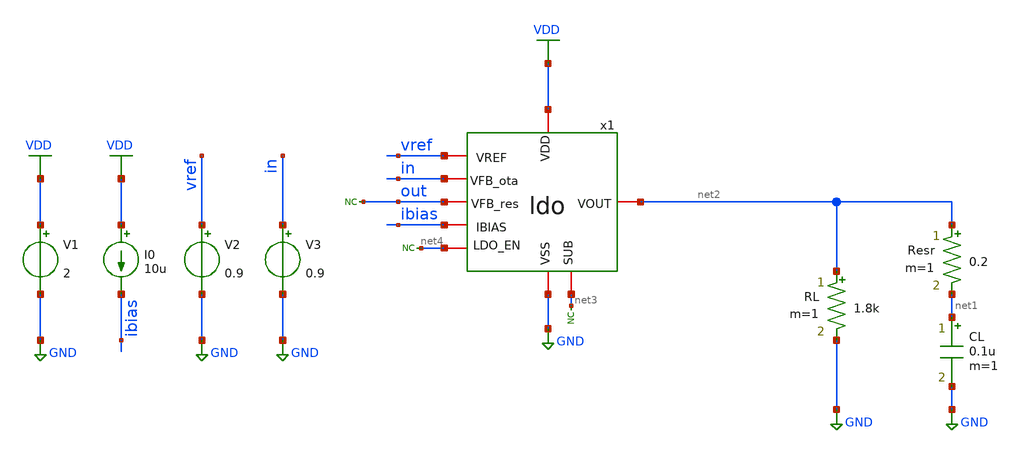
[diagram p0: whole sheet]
** sch_path: designs/libs/tb_ldo/tb_ldo/tb_ldo/tb_ldo_stb/tb_ldo_stb.sch
**.subckt tb_ldo_stb
RL net2 GND 1.8k m=1
V1 VDD GND 2
V2 vref GND 0.9
I0 VDD ibias 10u
CL net1 GND 0.1u m=1
Resr net2 net1 0.2 m=1
V3 in GND 0.9
* noconn out
x1 VDD vref net2 ibias net3 GND net4 in out ldo
* noconn #net3
* noconn #net4
**** begin user architecture code



.control
save all

run
set color0 = white

** Set sources
alter @V3[AC] = 1

** Simulations
ac dec 100 1 10G

** Plots
setplot ac1
let phase_deg = cph(-1*v(out))*180/pi
let phase_deg_ota = cph(v(x1.vota))*180/pi
plot phase_deg
plot phase_deg_ota

** Measurements
let gain_db = db(v(out))
meas ac f_0db WHEN gain_db = 0
meas ac phase_0db FIND phase_deg WHEN gain_db = 0
let phase_margin = 180 + phase_0db
print phase_margin

write tb_ldo_stb.raw
.endc
* ngspice commands




.include $::180MCU_MODELS/design.ngspice
.lib $::180MCU_MODELS/sm141064.ngspice typical
.lib $::180MCU_MODELS/sm141064.ngspice cap_mim
.lib $::180MCU_MODELS/sm141064.ngspice moscap_typical
.lib $::180MCU_MODELS/sm141064.ngspice mimcap_typical
.lib $::180MCU_MODELS/sm141064.ngspice res_typical
* .lib $::180MCU_MODELS/sm141064.ngspice res_statistical
* ngspice commands

**** end user architecture code
**.ends
.GLOBAL GND
.GLOBAL VDD
.end
